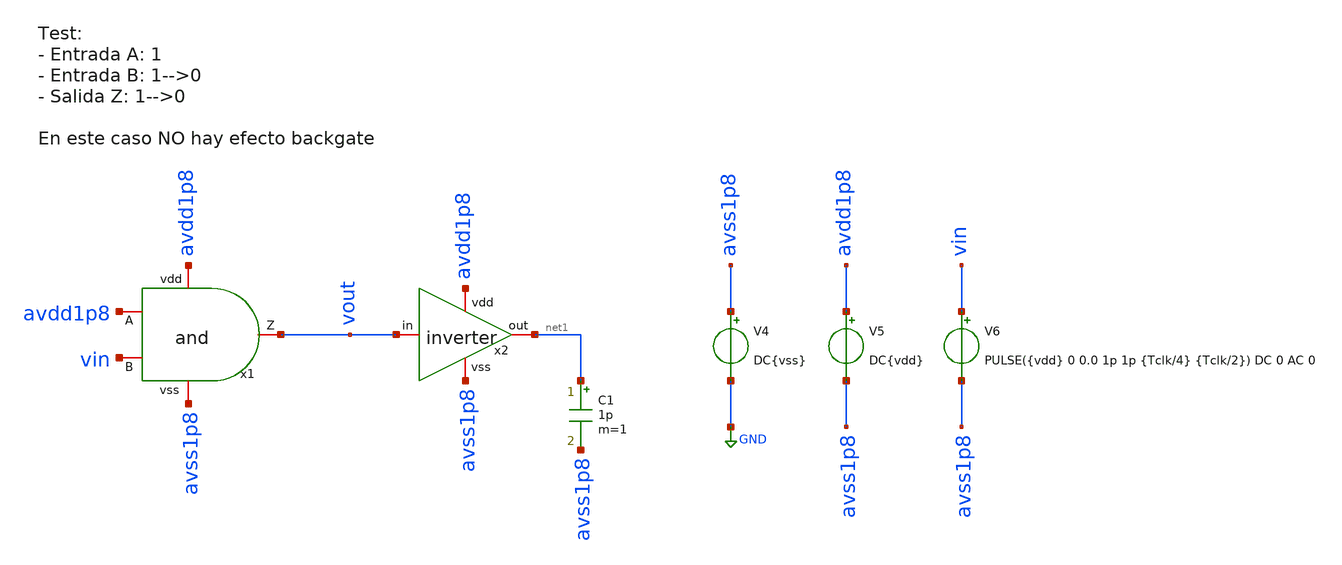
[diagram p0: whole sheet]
** sch_path: designs/sch/tests/test4_and.sch
**.subckt test4_and
x2 avdd1p8 net1 vout avss1p8 inverter
V4 avss1p8 GND DC{vss}
V5 avdd1p8 avss1p8 DC{vdd}
V6 vin avss1p8 PULSE({vdd} 0 0.0 1p 1p {Tclk/4} {Tclk/2}) DC 0 AC 0
C1 net1 avss1p8 1p m=1
x1 avdd1p8 avdd1p8 vout vin avss1p8 and
**** begin user architecture code


* Circuit Parameters
.param vdd = 1.8
.param vss = 0.0
.param Tclk = 10n
.options TEMP = 65.0

* Include Models
.lib /foss/pdks/sky130A/libs.tech/ngspice/sky130.lib.spice TT

* OP Parameters & Singals to save
.save all

* Simulations
.control
  tran 0.01u 100n
  setplot tran1
  plot v(vin) v(vout)+2
reset
  dc V6 0 1.8 0.01
  setplot dc
  plot vin vout ylabel vout xlabel vin
  set filetype = ascii
  write dcsweep.raw
.endc

.end


**** end user architecture code
**.ends

* expanding   symbol:  /foss/designs/sch/inverter.sym # of pins=4
** sym_path: designs/inverter.sym
** sch_path: designs/inverter.sch
.subckt inverter vdd out in vss
*.iopin out
*.iopin vss
*.iopin vdd
*.iopin in
XM2 out in vss vss sky130_fd_pr__nfet_01v8 L=0.15 W=0.75 nf=1 ad='int((nf+1)/2) * W/nf * 0.29' as='int((nf+2)/2) * W/nf * 0.29'
+ pd='2*int((nf+1)/2) * (W/nf + 0.29)' ps='2*int((nf+2)/2) * (W/nf + 0.29)' nrd='0.29 / W' nrs='0.29 / W'
+ sa=0 sb=0 sd=0 mult=1 m=1
XM1 out in vdd vdd sky130_fd_pr__pfet_01v8 L=0.15 W=1.5 nf=1 ad='int((nf+1)/2) * W/nf * 0.29' as='int((nf+2)/2) * W/nf * 0.29'
+ pd='2*int((nf+1)/2) * (W/nf + 0.29)' ps='2*int((nf+2)/2) * (W/nf + 0.29)' nrd='0.29 / W' nrs='0.29 / W'
+ sa=0 sb=0 sd=0 mult=1 m=1
.ends


* expanding   symbol:  /foss/designs/sch/and.sym # of pins=5
** sym_path: designs/and.sym
** sch_path: designs/and.sch
.subckt and vdd A Z B vss
*.iopin Z
*.iopin A
*.iopin B
*.iopin vdd
*.iopin vss
x1 vdd net1 A B vss nand
x2 vdd Z net1 vss inverter
.ends


* expanding   symbol:  /foss/designs/nand.sym # of pins=5
** sym_path: designs/nand.sym
** sch_path: designs/nand.sch
.subckt nand vdd Z A B vss
*.iopin B
*.iopin A
*.iopin vdd
*.iopin Z
*.iopin vss
XM1 net1 B vss vss sky130_fd_pr__nfet_01v8 L=0.15 W=1.5 nf=1 ad='int((nf+1)/2) * W/nf * 0.29' as='int((nf+2)/2) * W/nf * 0.29'
+ pd='2*int((nf+1)/2) * (W/nf + 0.29)' ps='2*int((nf+2)/2) * (W/nf + 0.29)' nrd='0.29 / W' nrs='0.29 / W'
+ sa=0 sb=0 sd=0 mult=1 m=1
XM2 Z A net1 vss sky130_fd_pr__nfet_01v8 L=0.15 W=1.5 nf=1 ad='int((nf+1)/2) * W/nf * 0.29' as='int((nf+2)/2) * W/nf * 0.29'
+ pd='2*int((nf+1)/2) * (W/nf + 0.29)' ps='2*int((nf+2)/2) * (W/nf + 0.29)' nrd='0.29 / W' nrs='0.29 / W'
+ sa=0 sb=0 sd=0 mult=1 m=1
XM3 Z A vdd vdd sky130_fd_pr__pfet_01v8 L=0.15 W=1.5 nf=1 ad='int((nf+1)/2) * W/nf * 0.29' as='int((nf+2)/2) * W/nf * 0.29'
+ pd='2*int((nf+1)/2) * (W/nf + 0.29)' ps='2*int((nf+2)/2) * (W/nf + 0.29)' nrd='0.29 / W' nrs='0.29 / W'
+ sa=0 sb=0 sd=0 mult=1 m=1
XM4 Z B vdd vdd sky130_fd_pr__pfet_01v8 L=0.15 W=1.5 nf=1 ad='int((nf+1)/2) * W/nf * 0.29' as='int((nf+2)/2) * W/nf * 0.29'
+ pd='2*int((nf+1)/2) * (W/nf + 0.29)' ps='2*int((nf+2)/2) * (W/nf + 0.29)' nrd='0.29 / W' nrs='0.29 / W'
+ sa=0 sb=0 sd=0 mult=1 m=1
.ends

.GLOBAL GND
.end
